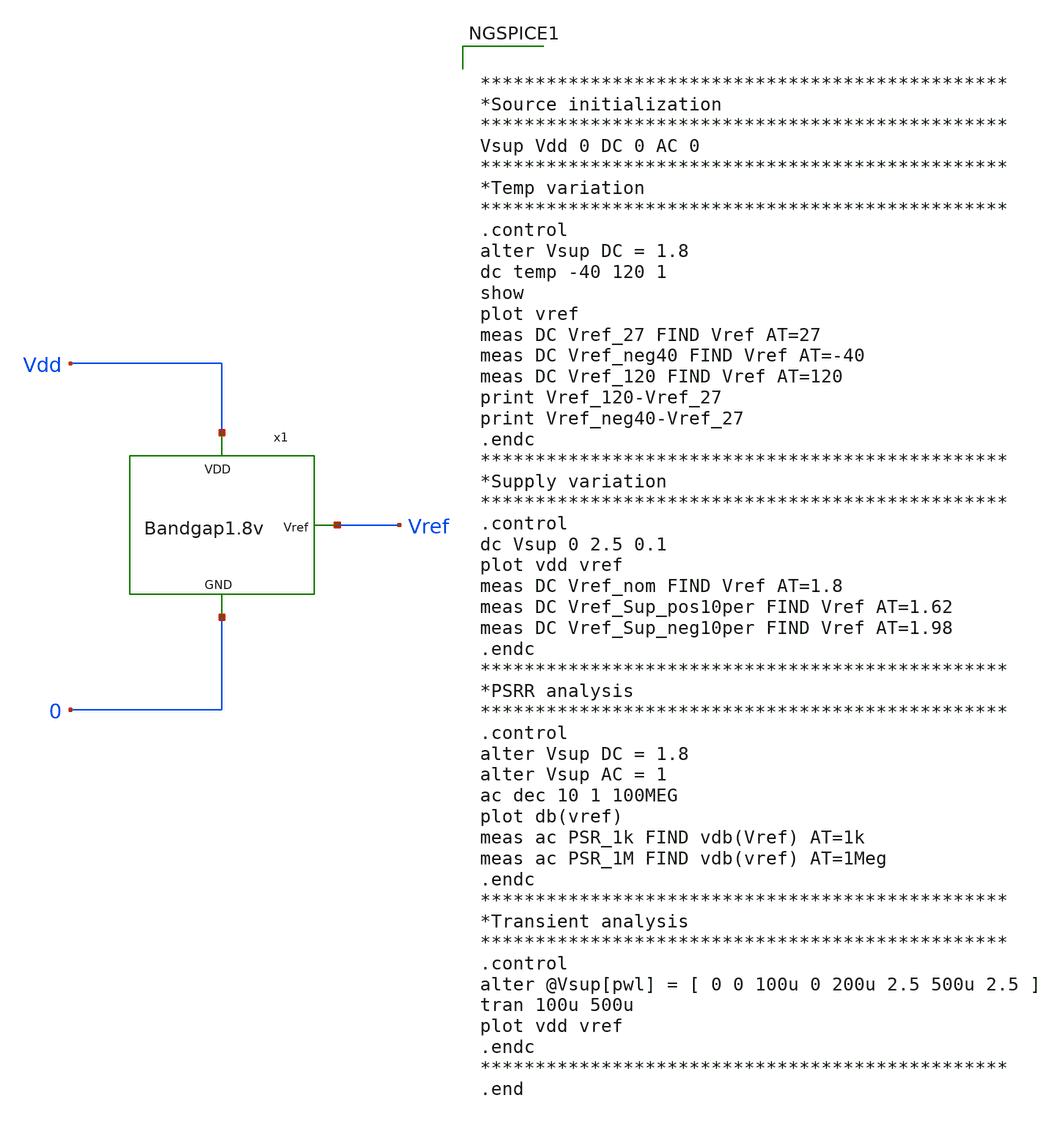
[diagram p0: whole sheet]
** sch_path: Analog_Blocks/Bandgap/Testbench/Bandgap1.8v_meas.sch
**.subckt Bandgap1.8v_meas
x1 Vref Vdd 0 Bandgap1.8v
**** begin user architecture code


************************************************
*Source initialization
************************************************
Vsup Vdd 0 DC 0 AC 0
************************************************
*Temp variation
************************************************
.control
alter Vsup DC = 1.8
dc temp -40 120 1
show
plot vref
meas DC Vref_27 FIND Vref AT=27
meas DC Vref_neg40 FIND Vref AT=-40
meas DC Vref_120 FIND Vref AT=120
print Vref_120-Vref_27
print Vref_neg40-Vref_27
.endc
************************************************
*Supply variation
************************************************
.control
dc Vsup 0 2.5 0.1
plot vdd vref
meas DC Vref_nom FIND Vref AT=1.8
meas DC Vref_Sup_pos10per FIND Vref AT=1.62
meas DC Vref_Sup_neg10per FIND Vref AT=1.98
.endc
************************************************
*PSRR analysis
************************************************
.control
alter Vsup DC = 1.8
alter Vsup AC = 1
ac dec 10 1 100MEG
plot db(vref)
meas ac PSR_1k FIND vdb(Vref) AT=1k
meas ac PSR_1M FIND vdb(vref) AT=1Meg
.endc
************************************************
*Transient analysis
************************************************
.control
alter @Vsup[pwl] = [ 0 0 100u 0 200u 2.5 500u 2.5 ]
tran 100u 500u
plot vdd vref
.endc
************************************************
.end



.include ~/Analog_blocks/models/skywater-pdk/libraries/sky130_fd_pr/latest/cells/nfet_01v8/sky130_fd_pr__nfet_01v8__tt.corner.spice
.include ~/Analog_blocks/models/skywater-pdk/libraries/sky130_fd_pr/latest/cells/nfet_01v8_lvt/sky130_fd_pr__nfet_01v8_lvt__tt.corner.spice
.include ~/Analog_blocks/models/skywater-pdk/libraries/sky130_fd_pr/latest/cells/pfet_01v8/sky130_fd_pr__pfet_01v8__tt.corner.spice
.include ~/Analog_blocks/models/skywater-pdk/libraries/sky130_fd_pr/latest/cells/nfet_03v3_nvt/sky130_fd_pr__nfet_03v3_nvt__tt.corner.spice
.include ~/Analog_blocks/models/skywater-pdk/libraries/sky130_fd_pr/latest/cells/nfet_05v0_nvt/sky130_fd_pr__nfet_05v0_nvt__tt.corner.spice
.include ~/Analog_blocks/models/skywater-pdk/libraries/sky130_fd_pr/latest/cells/esd_nfet_01v8/sky130_fd_pr__esd_nfet_01v8__tt.corner.spice
.include ~/Analog_blocks/models/skywater-pdk/libraries/sky130_fd_pr/latest/cells/pfet_01v8_lvt/sky130_fd_pr__pfet_01v8_lvt__tt.corner.spice
.include ~/Analog_blocks/models/skywater-pdk/libraries/sky130_fd_pr/latest/cells/pfet_01v8_hvt/sky130_fd_pr__pfet_01v8_hvt__tt.corner.spice
.include ~/Analog_blocks/models/skywater-pdk/libraries/sky130_fd_pr/latest/cells/esd_pfet_g5v0d10v5/sky130_fd_pr__esd_pfet_g5v0d10v5__tt.corner.spice
.include ~/Analog_blocks/models/skywater-pdk/libraries/sky130_fd_pr/latest/cells/pfet_g5v0d10v5/sky130_fd_pr__pfet_g5v0d10v5__tt.corner.spice
.include ~/Analog_blocks/models/skywater-pdk/libraries/sky130_fd_pr/latest/cells/pfet_g5v0d16v0/sky130_fd_pr__pfet_g5v0d16v0__tt.corner.spice
.include ~/Analog_blocks/models/skywater-pdk/libraries/sky130_fd_pr/latest/cells/nfet_g5v0d10v5/sky130_fd_pr__nfet_g5v0d10v5__tt.corner.spice
.include ~/Analog_blocks/models/skywater-pdk/libraries/sky130_fd_pr/latest/cells/nfet_g5v0d16v0/sky130_fd_pr__nfet_g5v0d16v0__tt_discrete.corner.spice
.include ~/Analog_blocks/models/skywater-pdk/libraries/sky130_fd_pr/latest/cells/esd_nfet_g5v0d10v5/sky130_fd_pr__esd_nfet_g5v0d10v5__tt.corner.spice
.include ~/Analog_blocks/models/skywater-pdk/libraries/sky130_fd_pr/latest/models/corners/tt/nonfet.spice
* Mismatch parameters
.include ~/Analog_blocks/models/skywater-pdk/libraries/sky130_fd_pr/latest/cells/nfet_01v8/sky130_fd_pr__nfet_01v8__mismatch.corner.spice
.include ~/Analog_blocks/models/skywater-pdk/libraries/sky130_fd_pr/latest/cells/pfet_01v8/sky130_fd_pr__pfet_01v8__mismatch.corner.spice
.include ~/Analog_blocks/models/skywater-pdk/libraries/sky130_fd_pr/latest/cells/nfet_01v8_lvt/sky130_fd_pr__nfet_01v8_lvt__mismatch.corner.spice
.include ~/Analog_blocks/models/skywater-pdk/libraries/sky130_fd_pr/latest/cells/pfet_01v8_lvt/sky130_fd_pr__pfet_01v8_lvt__mismatch.corner.spice
.include ~/Analog_blocks/models/skywater-pdk/libraries/sky130_fd_pr/latest/cells/pfet_01v8_hvt/sky130_fd_pr__pfet_01v8_hvt__mismatch.corner.spice
.include ~/Analog_blocks/models/skywater-pdk/libraries/sky130_fd_pr/latest/cells/nfet_g5v0d10v5/sky130_fd_pr__nfet_g5v0d10v5__mismatch.corner.spice
.include ~/Analog_blocks/models/skywater-pdk/libraries/sky130_fd_pr/latest/cells/pfet_g5v0d10v5/sky130_fd_pr__pfet_g5v0d10v5__mismatch.corner.spice
.include ~/Analog_blocks/models/skywater-pdk/libraries/sky130_fd_pr/latest/cells/nfet_05v0_nvt/sky130_fd_pr__nfet_05v0_nvt__mismatch.corner.spice
.include ~/Analog_blocks/models/skywater-pdk/libraries/sky130_fd_pr/latest/cells/nfet_03v3_nvt/sky130_fd_pr__nfet_03v3_nvt__mismatch.corner.spice
* Resistor
.include ~/Analog_blocks/models/skywater-pdk/libraries/sky130_fd_pr/latest/models/r+c/res_typical__cap_typical.spice
.include ~/Analog_blocks/models/skywater-pdk/libraries/sky130_fd_pr/latest/models/r+c/res_typical__cap_typical__lin.spice
* Special cells
.include ~/Analog_blocks/models/skywater-pdk/libraries/sky130_fd_pr/latest/models/corners/tt/specialized_cells.spice
* All models
.include ~/Analog_blocks/models/skywater-pdk/libraries/sky130_fd_pr/latest/models/all.spice
* Corner
.include ~/Analog_blocks/models/skywater-pdk/libraries/sky130_fd_pr/latest/models/corners/tt/rf.spice

**** end user architecture code
**.ends
.end
